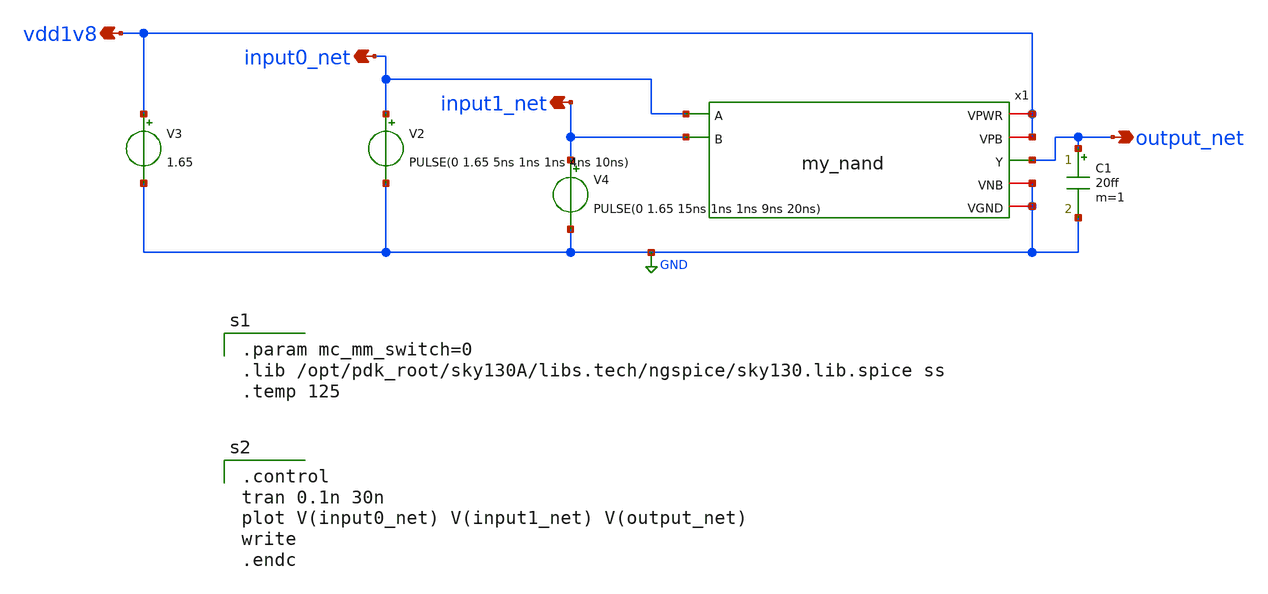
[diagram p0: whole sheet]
** sch_path: xschem/my_nand_tb.sch
**.subckt my_nand_tb input0_net vdd1v8 output_net input1_net
*.opin input0_net
*.opin vdd1v8
*.opin output_net
*.opin input1_net
V2 input0_net GND PULSE(0 1.65 5ns 1ns 1ns 4ns 10ns)
V3 vdd1v8 GND 1.65
V4 input1_net GND PULSE(0 1.65 15ns 1ns 1ns 9ns 20ns)
C1 output_net GND 20ff m=1
x1 vdd1v8 vdd1v8 input0_net output_net input1_net GND GND my_nand
**** begin user architecture code

.param mc_mm_switch=0
.lib /opt/pdk_root/sky130A/libs.tech/ngspice/sky130.lib.spice ss
.temp 125


.control
tran 0.1n 30n
plot V(input0_net) V(input1_net) V(output_net)
write
.endc

**** end user architecture code
**.ends

* expanding   symbol:  my_nand.sym # of pins=7
** sym_path: xschem/my_nand.sym
** sch_path: xschem/my_nand.sch
.subckt my_nand VPWR VPB A Y B VNB VGND
*.opin Y
*.ipin A
*.iopin VPWR
*.ipin B
*.iopin VGND
*.iopin VPB
*.iopin VNB
XM1 Y B net1 VNB sky130_fd_pr__nfet_01v8 L=0.15 W=0.65 nf=1 ad='int((nf+1)/2) * W/nf * 0.29' as='int((nf+2)/2) * W/nf * 0.29'
+ pd='2*int((nf+1)/2) * (W/nf + 0.29)' ps='2*int((nf+2)/2) * (W/nf + 0.29)' nrd='0.29 / W' nrs='0.29 / W'
+ sa=0 sb=0 sd=0 mult=1 m=1
XM2 net1 A VGND VNB sky130_fd_pr__nfet_01v8 L=0.15 W=0.65 nf=1 ad='int((nf+1)/2) * W/nf * 0.29' as='int((nf+2)/2) * W/nf * 0.29'
+ pd='2*int((nf+1)/2) * (W/nf + 0.29)' ps='2*int((nf+2)/2) * (W/nf + 0.29)' nrd='0.29 / W' nrs='0.29 / W'
+ sa=0 sb=0 sd=0 mult=1 m=1
XM3 Y A VPWR VPB sky130_fd_pr__pfet_01v8 L=0.15 W=1 nf=1 ad='int((nf+1)/2) * W/nf * 0.29' as='int((nf+2)/2) * W/nf * 0.29'
+ pd='2*int((nf+1)/2) * (W/nf + 0.29)' ps='2*int((nf+2)/2) * (W/nf + 0.29)' nrd='0.29 / W' nrs='0.29 / W'
+ sa=0 sb=0 sd=0 mult=1 m=1
XM4 Y B VPWR VPB sky130_fd_pr__pfet_01v8 L=0.15 W=1 nf=1 ad='int((nf+1)/2) * W/nf * 0.29' as='int((nf+2)/2) * W/nf * 0.29'
+ pd='2*int((nf+1)/2) * (W/nf + 0.29)' ps='2*int((nf+2)/2) * (W/nf + 0.29)' nrd='0.29 / W' nrs='0.29 / W'
+ sa=0 sb=0 sd=0 mult=1 m=1
.ends

.GLOBAL GND
.end
